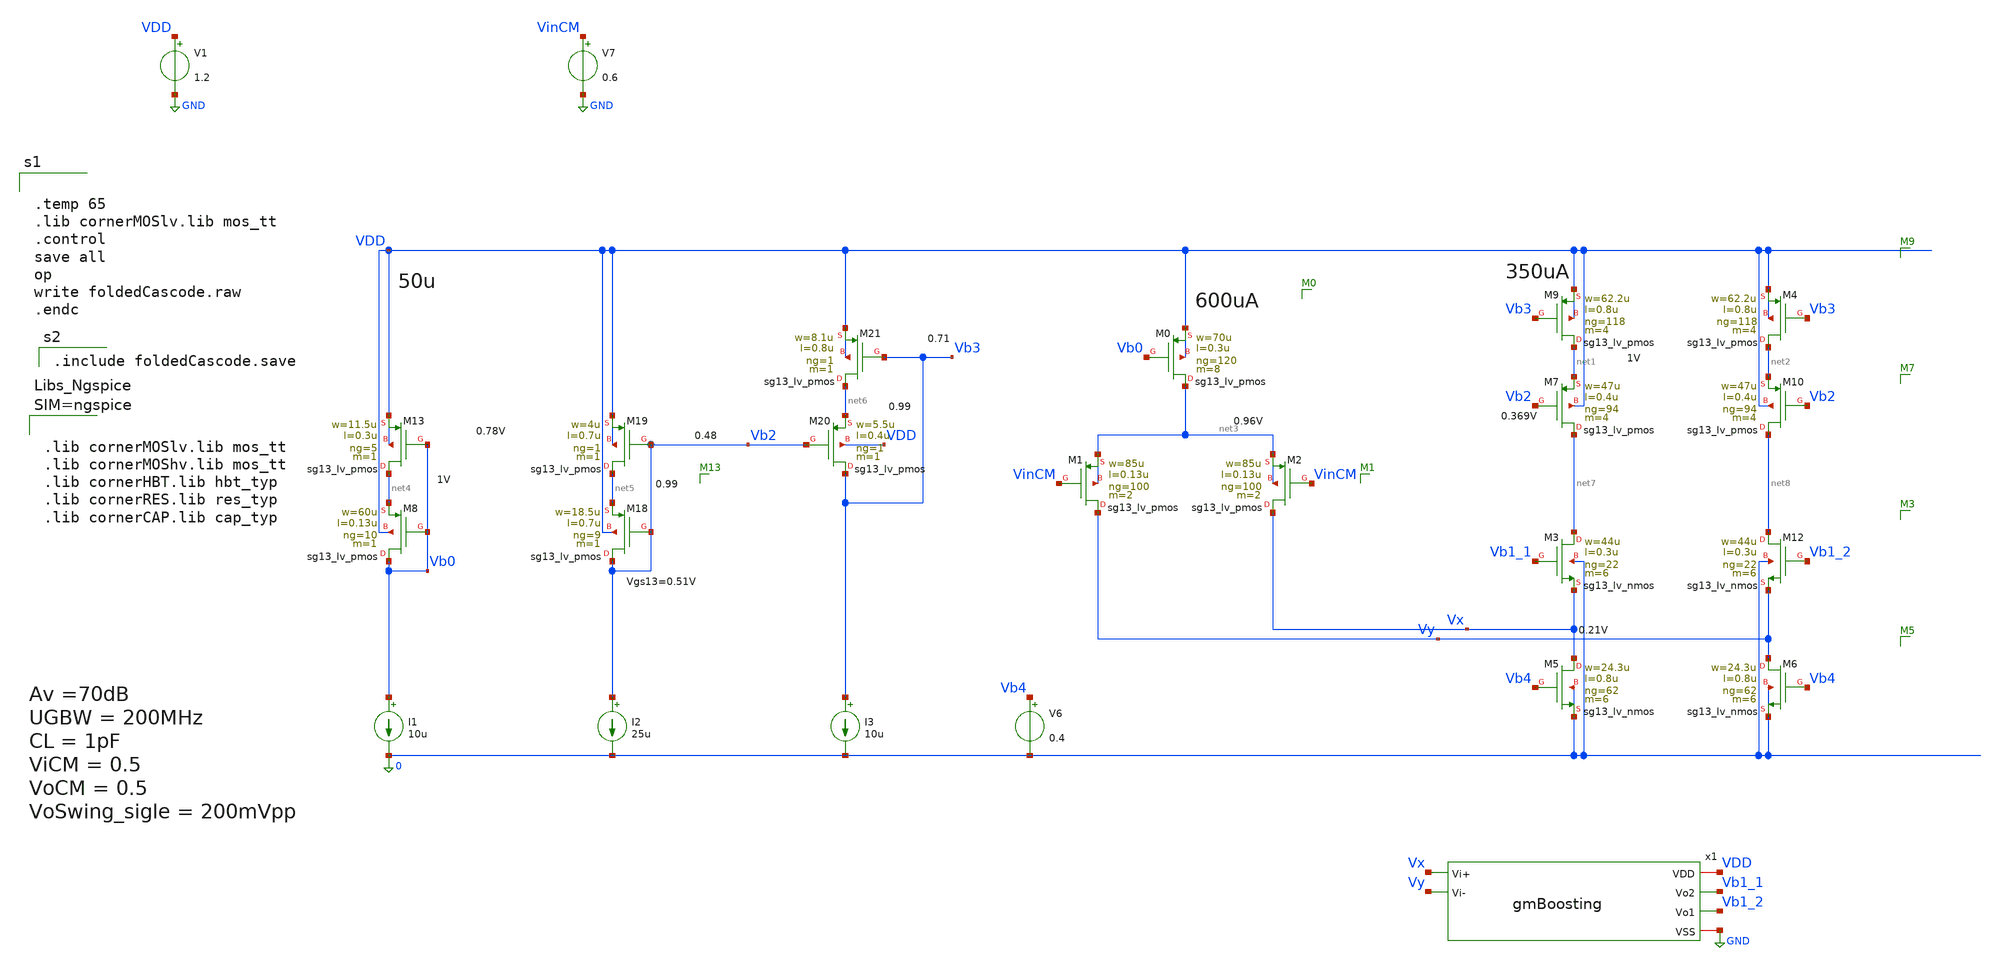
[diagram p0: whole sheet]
** sch_path: sch/testing/foldedCascode.sch
**.subckt foldedCascode
V1 VDD GND 1.2
XM5 Vx Vb4 0 0 sg13_lv_nmos w=24.3u l=0.8u ng=62 m=6 mm_ok=1
XM6 Vy Vb4 0 0 sg13_lv_nmos w=24.3u l=0.8u ng=62 m=6 mm_ok=1
XM9 net1 Vb3 VDD VDD sg13_lv_pmos w=62.2u l=0.8u ng=118 m=4 mm_ok=1
V7 VinCM GND 0.6
XM1 Vy VinCM net3 net3 sg13_lv_pmos w=85u l=0.13u ng=100 m=2 mm_ok=1
XM0 net3 Vb0 VDD VDD sg13_lv_pmos w=70u l=0.3u ng=120 m=8 mm_ok=1
x1 VDD Vb1_1 Vb1_2 Vx Vy GND gmBoosting
XM7 net7 Vb2 net1 VDD sg13_lv_pmos w=47u l=0.4u ng=94 m=4 mm_ok=1
XM2 Vx VinCM net3 net3 sg13_lv_pmos w=85u l=0.13u ng=100 m=2 mm_ok=1
XM4 net2 Vb3 VDD VDD sg13_lv_pmos w=62.2u l=0.8u ng=118 m=4 mm_ok=1
XM10 net8 Vb2 net2 VDD sg13_lv_pmos w=47u l=0.4u ng=94 m=4 mm_ok=1
V6 Vb4 0 0.4
XM3 net7 Vb1_1 Vx 0 sg13_lv_nmos w=44u l=0.3u ng=22 m=6 mm_ok=1
XM12 net8 Vb1_2 Vy 0 sg13_lv_nmos w=44u l=0.3u ng=22 m=6 mm_ok=1
I1 Vb0 0 10u
XM8 Vb0 Vb0 net4 VDD sg13_lv_pmos w=60u l=0.13u ng=10 m=1 mm_ok=1
XM13 net4 Vb0 VDD VDD sg13_lv_pmos w=11.5u l=0.3u ng=5 m=1 mm_ok=1
I2 Vb2 0 25u
XM18 Vb2 Vb2 net5 VDD sg13_lv_pmos w=18.5u l=0.7u ng=9 m=1 mm_ok=1
XM19 net5 Vb2 VDD VDD sg13_lv_pmos w=4u l=0.7u ng=1 m=1 mm_ok=1
XM20 Vb3 Vb2 net6 VDD sg13_lv_pmos w=5.5u l=0.4u ng=1 m=1 mm_ok=1
XM21 net6 Vb3 VDD VDD sg13_lv_pmos w=8.1u l=0.8u ng=1 m=1 mm_ok=1
I3 Vb3 0 10u
**** begin user architecture code


.temp 65
.lib cornerMOSlv.lib mos_tt
.control
save all
op
write foldedCascode.raw
.endc



.include foldedCascode.save




.lib cornerMOSlv.lib mos_tt
.lib cornerMOShv.lib mos_tt
.lib cornerHBT.lib hbt_typ
.lib cornerRES.lib res_typ
.lib cornerCAP.lib cap_typ



**** end user architecture code
**.ends

* expanding   symbol:  gmBoosting.sym # of pins=6
** sym_path: sch/blocks/gmBoosting.sym
** sch_path: sch/blocks/gmBoosting.sch
.subckt gmBoosting VDD Vo2 Vo1 Vi+ Vi- VSS
*.iopin VSS
*.opin Vo1
*.opin Vo2
*.ipin Vi+
*.ipin Vi-
*.iopin VDD
V1 Vref VSS 0.55
XM7 net2 Vb4 VDD VDD sg13_lv_pmos w=25u l=0.7u ng=13 m=2 mm_ok=1
XM1 net8 Vi+ net1 net1 sg13_lv_pmos w=40u l=0.15u ng=80 m=4 mm_ok=1
XM2 net4 Vi- net1 net1 sg13_lv_pmos w=40u l=0.15u ng=80 m=4 mm_ok=1
XM0 net1 Vb0 net5 VDD sg13_lv_pmos w=16u l=0.3u ng=20 m=1 mm_ok=1
XM6 net8 Vb3 VSS VSS sg13_lv_nmos w=20u l=0.7u ng=5 m=2 mm_ok=1
XM9 Vo1 Vb2 net2 VDD sg13_lv_pmos w=30u l=0.3u ng=10 m=1 mm_ok=1
XM10 Vo2 Vb2 net3 VDD sg13_lv_pmos w=30u l=0.3u ng=10 m=1 mm_ok=1
XM8 net3 Vb4 VDD VDD sg13_lv_pmos w=25u l=0.7u ng=13 m=2 mm_ok=1
XM3 net5 Vo2 VDD VDD sg13_lv_pmos w=20u l=0.13u ng=5 m=1 mm_ok=1
XM4 net5 Vo1 VDD VDD sg13_lv_pmos w=20u l=0.13u ng=5 m=1 mm_ok=1
XM5 net6 Vref VDD VDD sg13_lv_pmos w=20u l=0.13u ng=5 m=2 mm_ok=1
XM28 Vb0 net7 VSS VSS sg13_lv_nmos w=10u l=0.2u ng=2 m=1 mm_ok=1
XM29 Vb3 Vb3 VSS VSS sg13_lv_nmos w=30u l=0.2u ng=4 m=1 mm_ok=1
XR16 net7 Vb0 sub! rppd w=0.8e-6 l=2.5e-6 m=1 b=0 mm_ok=1
XM30 Vb3 Vb0 net6 VDD sg13_lv_pmos w=16u l=0.3u ng=20 m=1 mm_ok=1
XM31 net4 Vb3 VSS VSS sg13_lv_nmos w=20u l=0.7u ng=5 m=2 mm_ok=1
XM32 Vo1 Vb1 net4 VSS sg13_lv_nmos w=37.5u l=0.7u ng=5 m=1 mm_ok=1
XM33 Vo2 Vb1 net8 VSS sg13_lv_nmos w=37.5u l=0.7u ng=5 m=1 mm_ok=1
XM23 net7 Vbb VDD VDD sg13_lv_pmos w=18u l=1u ng=18 m=1 mm_ok=1
XR9 Vb1 net10 sub! rhigh w=0.5e-6 l=2.31e-6 m=1 b=0 mm_ok=1
XM17 net10 Vb1 net9 VSS sg13_lv_nmos w=25u l=0.7u ng=3 m=1 mm_ok=1
XM18 net9 net10 VSS VSS sg13_lv_nmos w=40u l=0.7u ng=4 m=1 mm_ok=1
XM19 net11 Vb4 VDD VDD sg13_lv_pmos w=15u l=0.7u ng=5 m=1 mm_ok=1
XM20 Vb4 Vb2 net11 VDD sg13_lv_pmos w=7u l=0.3u ng=7 m=1 mm_ok=1
XR10 Vb4 Vb2 sub! rhigh w=0.5e-6 l=1.8e-6 m=1 b=0 mm_ok=1
I3 Vbb VSS 50u
XM21 Vbb Vbb VDD VDD sg13_lv_pmos w=18u l=1u ng=18 m=1 mm_ok=1
XM22 Vb1 Vbb VDD VDD sg13_lv_pmos w=18u l=1u ng=18 m=1 mm_ok=1
XM24 net12 Vbb VDD VDD sg13_lv_pmos w=18u l=1u ng=18 m=1 mm_ok=1
XM25 net12 net12 VSS VSS sg13_lv_nmos w=15u l=1u ng=2 m=1 mm_ok=1
XM26 Vb2 net12 VSS VSS sg13_lv_nmos w=15u l=1u ng=2 m=1 mm_ok=1
.ends

.GLOBAL GND
.end
